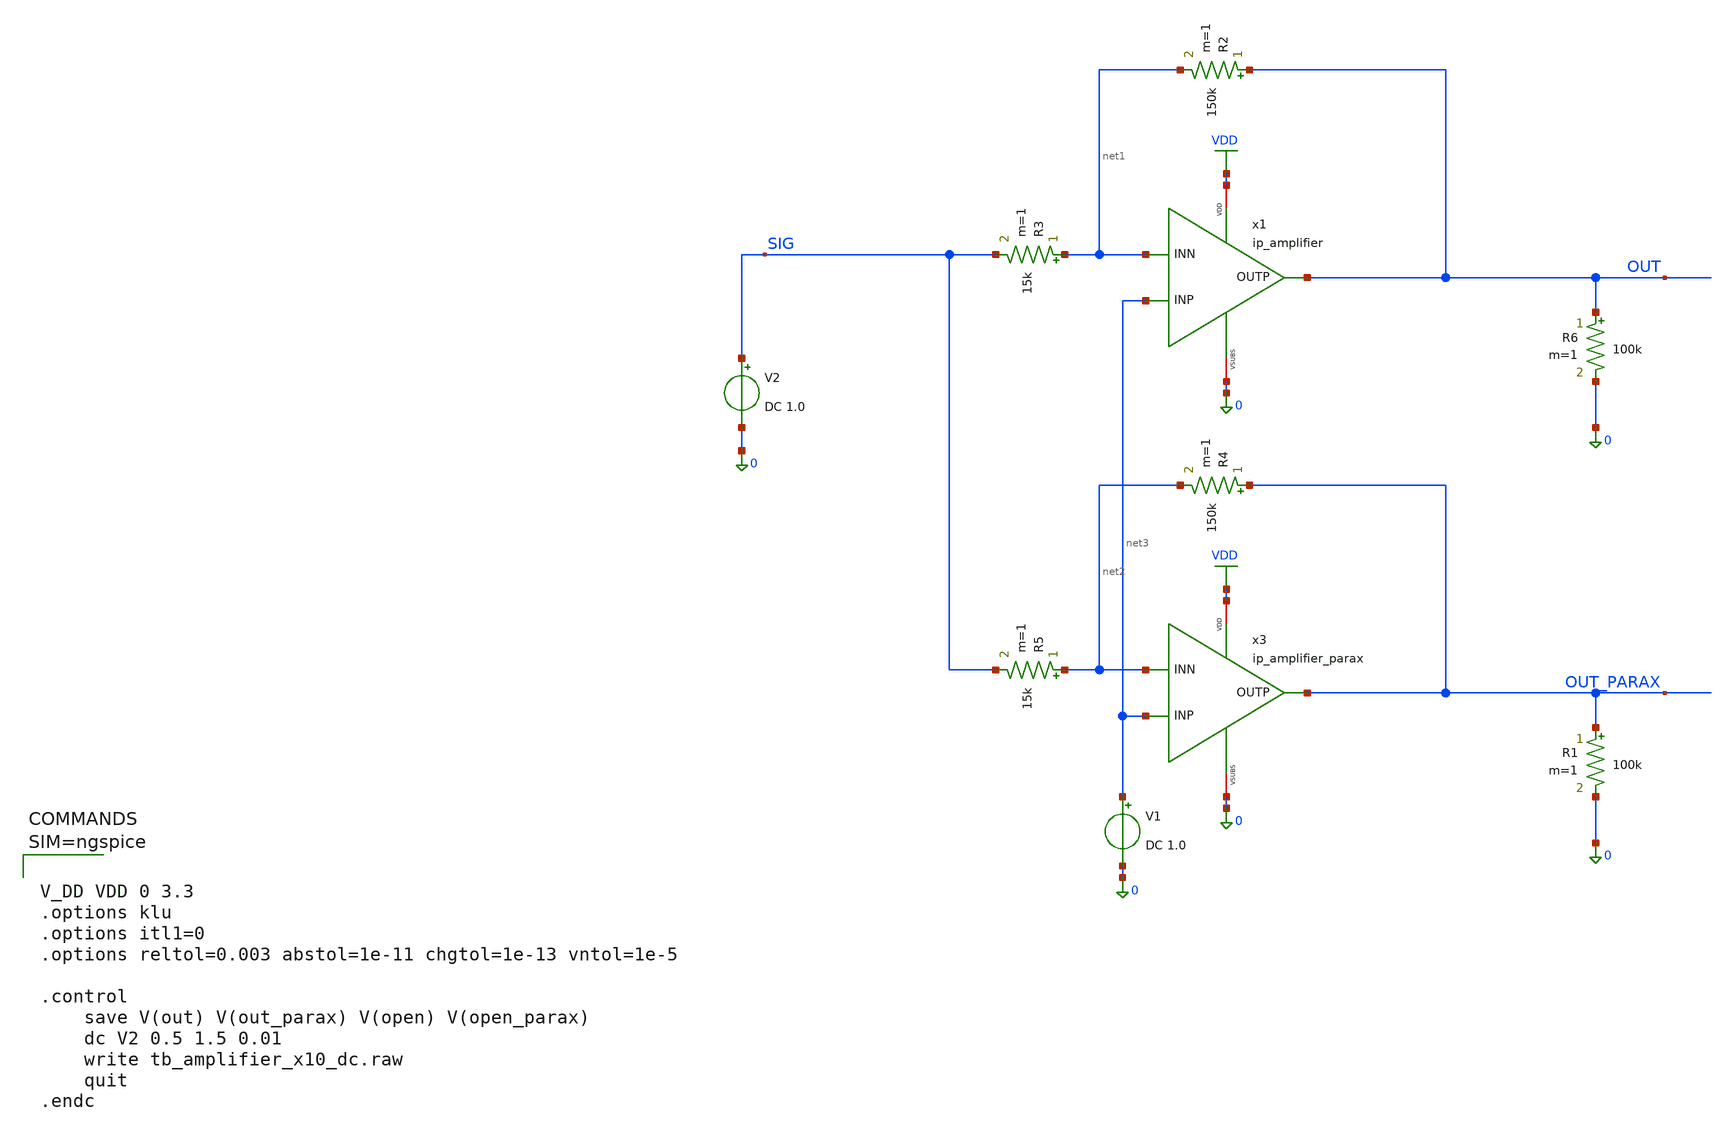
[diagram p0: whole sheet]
** sch_path: xschem/tb_amplifier_x10_dc.sch
**.subckt tb_amplifier_x10_dc
x1 VDD 0 net3 net1 OUT ip_amplifier
R6 OUT 0 100k m=1
V2 SIG 0 DC 1.0
R1 OUT_PARAX 0 100k m=1
x3 VDD 0 net3 net2 OUT_PARAX ip_amplifier_parax
R2 OUT net1 150k m=1
R3 net1 SIG 15k m=1
R4 OUT_PARAX net2 150k m=1
R5 net2 SIG 15k m=1
V1 net3 0 DC 1.0
**** begin user architecture code

.inc $::180MCU_MODELS/design.spice
.lib $::180MCU_MODELS/sm141064.ngspice typical
.lib $::180MCU_MODELS/sm141064.ngspice cap_mim
.lib $::180MCU_MODELS/sm141064.ngspice moscap_typical
.lib $::180MCU_MODELS/sm141064.ngspice diode_typical
.lib $::180MCU_MODELS/sm141064.ngspice res_typical
.lib $::180MCU_MODELS/sm141064.ngspice mimcap_typical




V_DD VDD 0 3.3
.options klu
.options itl1=0
.options reltol=0.003 abstol=1e-11 chgtol=1e-13 vntol=1e-5

.control
	save V(out) V(out_parax) V(open) V(open_parax)
	dc V2 0.5 1.5 0.01
	write tb_amplifier_x10_dc.raw
	quit
.endc



**** end user architecture code
**.ends

* expanding   symbol:  ip_amplifier.sym # of pins=5
** sym_path: ip_amplifier.sym
** sch_path: ip_amplifier.sch
.subckt ip_amplifier VDD VSUBS INP INN OUTP
*.iopin VDD
*.iopin VSUBS
*.ipin INP
*.ipin INN
*.opin OUTP
XM1 COMP INP COMMON_ VDD pfet_03v3 L=5u W=18.0u nf=1 ad='int((nf+1)/2) * W/nf * 0.18u' as='int((nf+2)/2) * W/nf * 0.18u'
+ pd='2*int((nf+1)/2) * (W/nf + 0.18u)' ps='2*int((nf+2)/2) * (W/nf + 0.18u)' nrd='0.18u / W' nrs='0.18u / W'
+ sa=0 sb=0 sd=0 m=1 par=1
XM2 net6 INN COMMON_ VDD pfet_03v3 L=5u W=18.0u nf=1 ad='int((nf+1)/2) * W/nf * 0.18u' as='int((nf+2)/2) * W/nf * 0.18u'
+ pd='2*int((nf+1)/2) * (W/nf + 0.18u)' ps='2*int((nf+2)/2) * (W/nf + 0.18u)' nrd='0.18u / W' nrs='0.18u / W'
+ sa=0 sb=0 sd=0 m=1 par=1
XM3 net2 NBIAS VSUBS vsubs nfet_03v3 L=2u W=6u nf=1 ad='int((nf+1)/2) * W/nf * 0.18u' as='int((nf+2)/2) * W/nf * 0.18u'
+ pd='2*int((nf+1)/2) * (W/nf + 0.18u)' ps='2*int((nf+2)/2) * (W/nf + 0.18u)' nrd='0.18u / W' nrs='0.18u / W'
+ sa=0 sb=0 sd=0 m=2 par=2
XM4 net1 NBIAS VSUBS vsubs nfet_03v3 L=2u W=6u nf=1 ad='int((nf+1)/2) * W/nf * 0.18u' as='int((nf+2)/2) * W/nf * 0.18u'
+ pd='2*int((nf+1)/2) * (W/nf + 0.18u)' ps='2*int((nf+2)/2) * (W/nf + 0.18u)' nrd='0.18u / W' nrs='0.18u / W'
+ sa=0 sb=0 sd=0 m=1 par=1
XM7 NBIAS NBIAS net2 vsubs nfet_03v3 L=0.5u W=6u nf=1 ad='int((nf+1)/2) * W/nf * 0.18u' as='int((nf+2)/2) * W/nf * 0.18u'
+ pd='2*int((nf+1)/2) * (W/nf + 0.18u)' ps='2*int((nf+2)/2) * (W/nf + 0.18u)' nrd='0.18u / W' nrs='0.18u / W'
+ sa=0 sb=0 sd=0 m=4 par=4
XM8 net3 NBIAS net1 vsubs nfet_03v3 L=0.5u W=6u nf=1 ad='int((nf+1)/2) * W/nf * 0.18u' as='int((nf+2)/2) * W/nf * 0.18u'
+ pd='2*int((nf+1)/2) * (W/nf + 0.18u)' ps='2*int((nf+2)/2) * (W/nf + 0.18u)' nrd='0.18u / W' nrs='0.18u / W'
+ sa=0 sb=0 sd=0 m=4 par=4
XM9 net4 PBIAS VDD VDD pfet_03v3 L=2u W=6u nf=1 ad='int((nf+1)/2) * W/nf * 0.18u' as='int((nf+2)/2) * W/nf * 0.18u'
+ pd='2*int((nf+1)/2) * (W/nf + 0.18u)' ps='2*int((nf+2)/2) * (W/nf + 0.18u)' nrd='0.18u / W' nrs='0.18u / W'
+ sa=0 sb=0 sd=0 m=1 par=1
XM10 net5 PBIAS VDD VDD pfet_03v3 L=2u W=6u nf=1 ad='int((nf+1)/2) * W/nf * 0.18u' as='int((nf+2)/2) * W/nf * 0.18u'
+ pd='2*int((nf+1)/2) * (W/nf + 0.18u)' ps='2*int((nf+2)/2) * (W/nf + 0.18u)' nrd='0.18u / W' nrs='0.18u / W'
+ sa=0 sb=0 sd=0 m=1 par=1
XM11 PBIAS PBIAS net4 VDD pfet_03v3 L=0.5u W=6u nf=1 ad='int((nf+1)/2) * W/nf * 0.18u' as='int((nf+2)/2) * W/nf * 0.18u'
+ pd='2*int((nf+1)/2) * (W/nf + 0.18u)' ps='2*int((nf+2)/2) * (W/nf + 0.18u)' nrd='0.18u / W' nrs='0.18u / W'
+ sa=0 sb=0 sd=0 m=4 par=4
XM12 COMMON PBIAS net5 VDD pfet_03v3 L=0.5u W=6u nf=1 ad='int((nf+1)/2) * W/nf * 0.18u' as='int((nf+2)/2) * W/nf * 0.18u'
+ pd='2*int((nf+1)/2) * (W/nf + 0.18u)' ps='2*int((nf+2)/2) * (W/nf + 0.18u)' nrd='0.18u / W' nrs='0.18u / W'
+ sa=0 sb=0 sd=0 m=4 par=4
XM13 COMP net6 VSUBS vsubs nfet_03v3 L=5u W=6u nf=1 ad='int((nf+1)/2) * W/nf * 0.18u' as='int((nf+2)/2) * W/nf * 0.18u'
+ pd='2*int((nf+1)/2) * (W/nf + 0.18u)' ps='2*int((nf+2)/2) * (W/nf + 0.18u)' nrd='0.18u / W' nrs='0.18u / W'
+ sa=0 sb=0 sd=0 m=1 par=1
XM14 net6 net6 VSUBS vsubs nfet_03v3 L=5u W=6u nf=1 ad='int((nf+1)/2) * W/nf * 0.18u' as='int((nf+2)/2) * W/nf * 0.18u'
+ pd='2*int((nf+1)/2) * (W/nf + 0.18u)' ps='2*int((nf+2)/2) * (W/nf + 0.18u)' nrd='0.18u / W' nrs='0.18u / W'
+ sa=0 sb=0 sd=0 m=1 par=1
XM17 net8 PBIAS VDD VDD pfet_03v3 L=0.5u W=12u nf=1 ad='int((nf+1)/2) * W/nf * 0.18u' as='int((nf+2)/2) * W/nf * 0.18u'
+ pd='2*int((nf+1)/2) * (W/nf + 0.18u)' ps='2*int((nf+2)/2) * (W/nf + 0.18u)' nrd='0.18u / W' nrs='0.18u / W'
+ sa=0 sb=0 sd=0 m=2 par=2
XM18 OUTP COMP VSUBS vsubs nfet_03v3 L=0.5u W=12u nf=1 ad='int((nf+1)/2) * W/nf * 0.18u' as='int((nf+2)/2) * W/nf * 0.18u'
+ pd='2*int((nf+1)/2) * (W/nf + 0.18u)' ps='2*int((nf+2)/2) * (W/nf + 0.18u)' nrd='0.18u / W' nrs='0.18u / W'
+ sa=0 sb=0 sd=0 m=4 par=4
XR3 NBIAS net7 vsubs ppolyf_u_1k r_width=1e-6 r_length=48e-6 m=1
Vmeas VDD net7 0
Vmeas1 PBIAS net3 0
Vmeas2 COMMON COMMON_ 0
Vmeas3 net8 OUTP 0
XC1 OUTP COMP cap_mim_2f0_m2m3_noshield c_width=10e-6 c_length=10e-6 m=2
.ends


* expanding   symbol:  ip_amplifier_parax.sym # of pins=5
** sym_path: ip_amplifier.sym
.include [file normalize ./parax/ip_amplifier.sim.spice]
.GLOBAL VDD
.end
